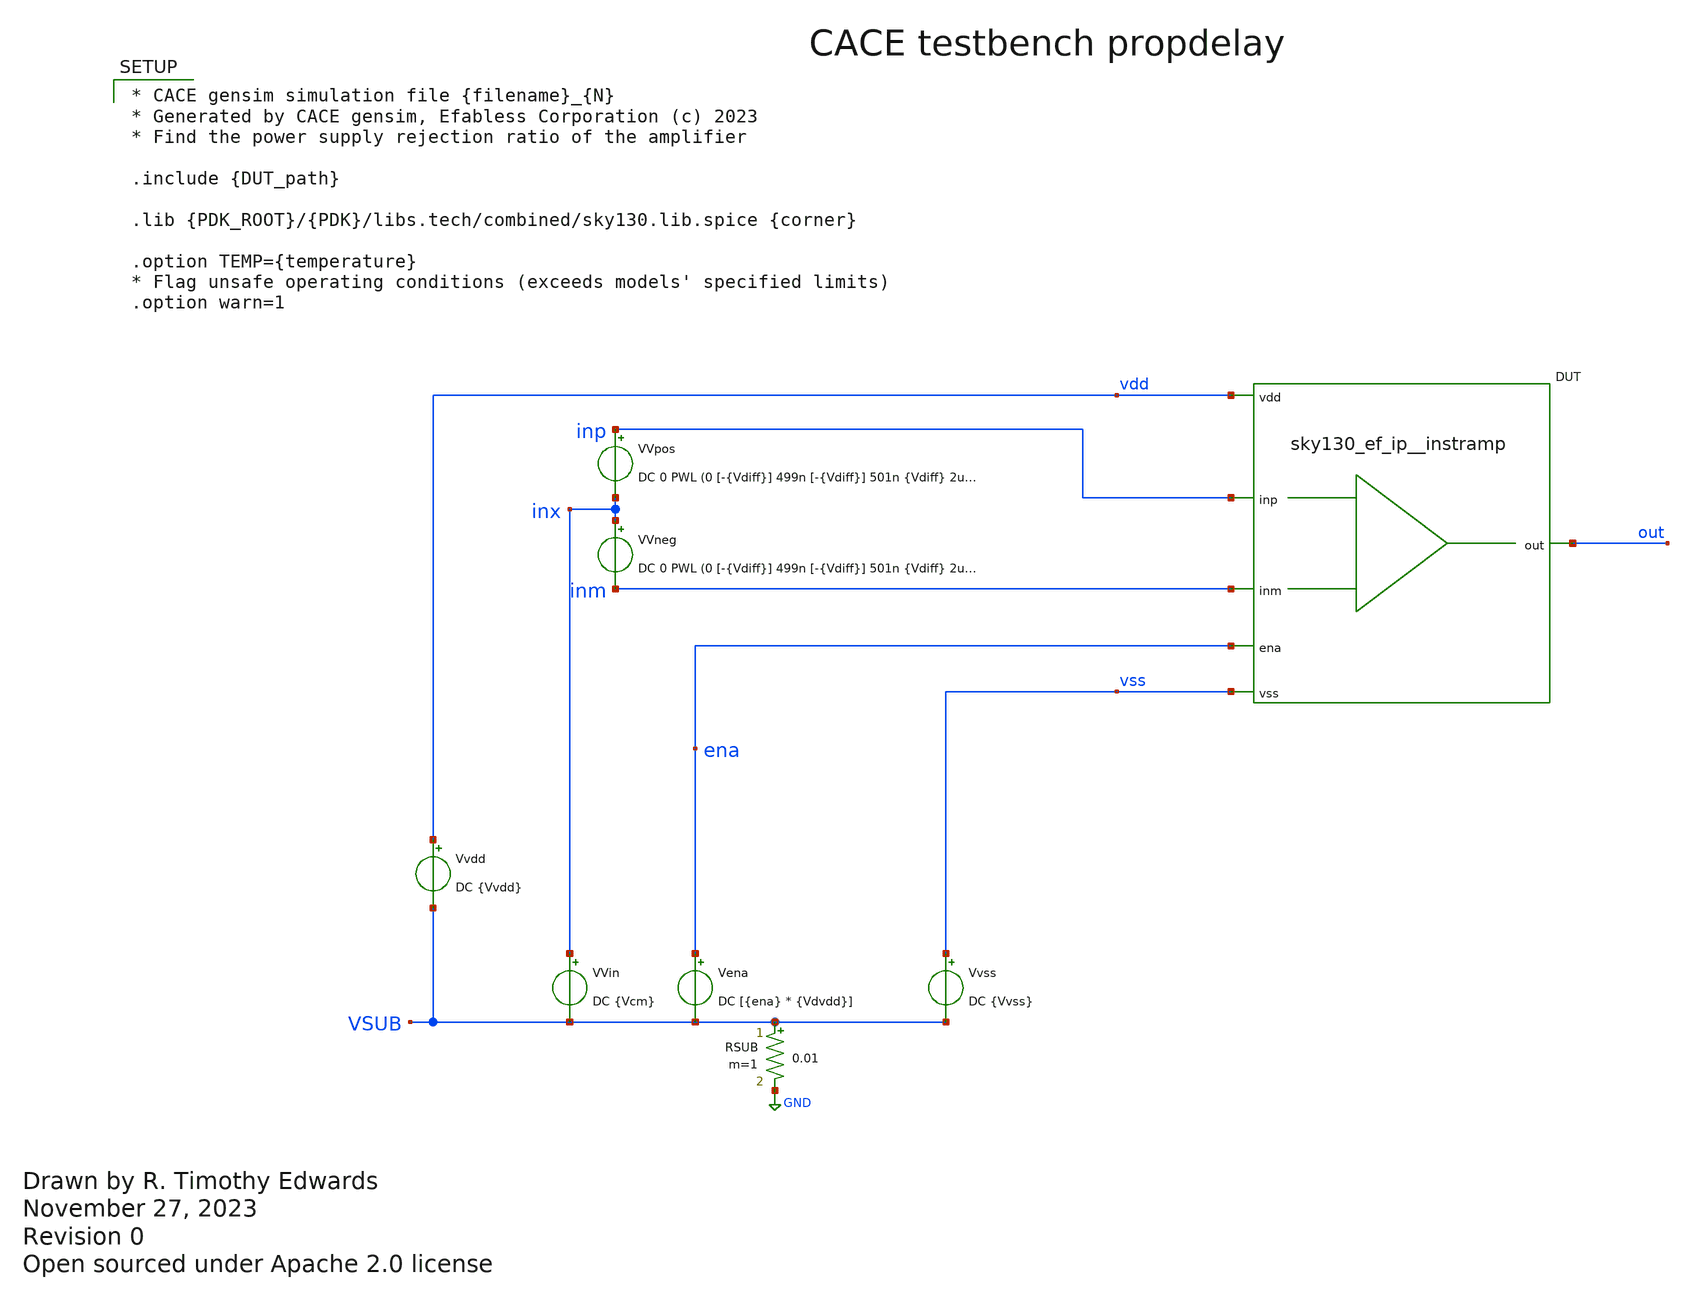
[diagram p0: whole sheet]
** sch_path: cace/propdelay.sch
* Open sourced under Apache 2.0 license
**.subckt propdelay
VVin inx VSUB DC {Vcm}
Vena ena VSUB DC [{ena} * {Vdvdd}]
Vvss vss VSUB DC {Vvss}
Vvdd vdd VSUB DC {Vvdd}
RSUB VSUB GND 0.01 m=1
XDUT {PIN|vdd|vdd} {PIN|vss|vss} {PIN|inm|inm} {PIN|inp|inp} {PIN|out|out} {PIN|ena|ena} {DUT_name}
VVpos inp inx DC 0 PWL (0 [-{Vdiff}] 499n [-{Vdiff}] 501n {Vdiff} 2u {Vdiff}
VVneg inx inm DC 0 PWL (0 [-{Vdiff}] 499n [-{Vdiff}] 501n {Vdiff} 2u {Vdiff}
**** begin user architecture code

.control
** Propagation delay.  Input differential Vdiff is set to the overdrive
** voltage.  Set this to the negative of its value, then switch to the
** positive.  Measure the time for the output to change state (cross
** Vdd / 2).
tran 1e-9 2e-6
meas tran trise WHEN V(out) = [{Vvdd} / 2] CROSS=1
let tpd = $&trise - 500e-9

set wr_singlescale
wrdata {simpath}/{filename}_{N}.data $&tpd
quit
.endc



* CACE gensim simulation file {filename}_{N}
* Generated by CACE gensim, Efabless Corporation (c) 2023
* Find the power supply rejection ratio of the amplifier

.include {DUT_path}

.lib {PDK_ROOT}/{PDK}/libs.tech/combined/sky130.lib.spice {corner}

.option TEMP={temperature}
* Flag unsafe operating conditions (exceeds models' specified limits)
.option warn=1


**** end user architecture code
**.ends
.GLOBAL GND
.end
